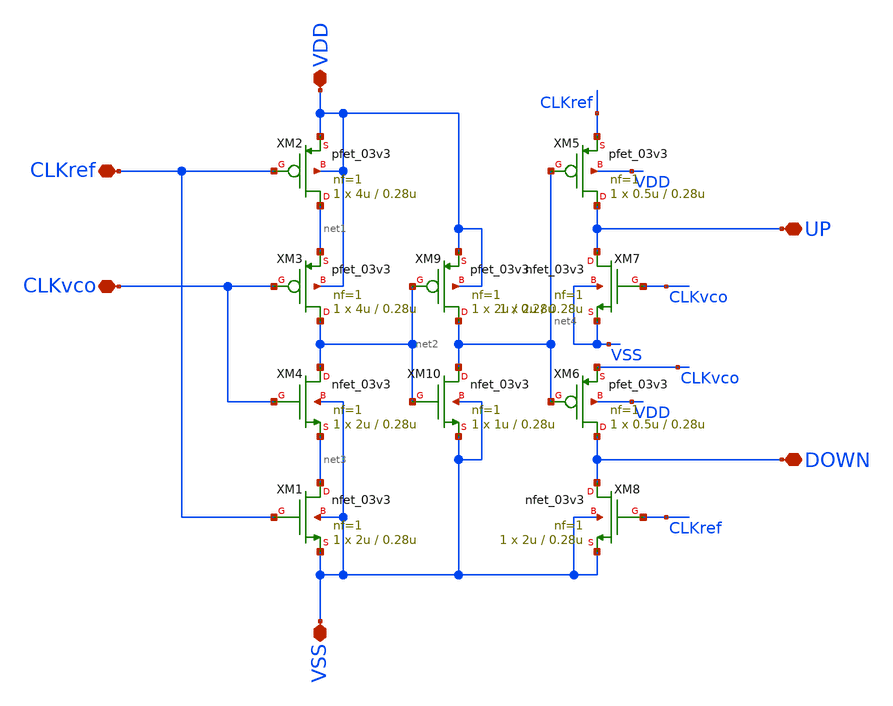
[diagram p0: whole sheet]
** sch_path: designs/libs/qw_core_analog/PFD_0deadzone.sch
**.subckt PFD_0deadzone CLKref CLKvco VSS VDD UP DOWN
*.iopin CLKref
*.iopin CLKvco
*.iopin VSS
*.iopin VDD
*.iopin UP
*.iopin DOWN
XM1 net3 CLKref VSS VSS nfet_03v3 L=0.28u W=2u nf=1 ad='int((nf+1)/2) * W/nf * 0.18u' as='int((nf+2)/2) * W/nf * 0.18u'
+ pd='2*int((nf+1)/2) * (W/nf + 0.18u)' ps='2*int((nf+2)/2) * (W/nf + 0.18u)' nrd='0.18u / W' nrs='0.18u / W'
+ sa=0 sb=0 sd=0 m=1
XM2 net1 CLKref VDD VDD pfet_03v3 L=0.28u W=4u nf=1 ad='int((nf+1)/2) * W/nf * 0.18u' as='int((nf+2)/2) * W/nf * 0.18u'
+ pd='2*int((nf+1)/2) * (W/nf + 0.18u)' ps='2*int((nf+2)/2) * (W/nf + 0.18u)' nrd='0.18u / W' nrs='0.18u / W'
+ sa=0 sb=0 sd=0 m=1
XM3 net2 CLKvco net1 VDD pfet_03v3 L=0.28u W=4u nf=1 ad='int((nf+1)/2) * W/nf * 0.18u' as='int((nf+2)/2) * W/nf * 0.18u'
+ pd='2*int((nf+1)/2) * (W/nf + 0.18u)' ps='2*int((nf+2)/2) * (W/nf + 0.18u)' nrd='0.18u / W' nrs='0.18u / W'
+ sa=0 sb=0 sd=0 m=1
XM4 net2 CLKvco net3 VSS nfet_03v3 L=0.28u W=2u nf=1 ad='int((nf+1)/2) * W/nf * 0.18u' as='int((nf+2)/2) * W/nf * 0.18u'
+ pd='2*int((nf+1)/2) * (W/nf + 0.18u)' ps='2*int((nf+2)/2) * (W/nf + 0.18u)' nrd='0.18u / W' nrs='0.18u / W'
+ sa=0 sb=0 sd=0 m=1
XM7 UP CLKvco VSS VSS nfet_03v3 L=0.28u W=2u nf=1 ad='int((nf+1)/2) * W/nf * 0.18u' as='int((nf+2)/2) * W/nf * 0.18u'
+ pd='2*int((nf+1)/2) * (W/nf + 0.18u)' ps='2*int((nf+2)/2) * (W/nf + 0.18u)' nrd='0.18u / W' nrs='0.18u / W'
+ sa=0 sb=0 sd=0 m=1
XM8 DOWN CLKref VSS VSS nfet_03v3 L=0.28u W=2u nf=1 ad='int((nf+1)/2) * W/nf * 0.18u' as='int((nf+2)/2) * W/nf * 0.18u'
+ pd='2*int((nf+1)/2) * (W/nf + 0.18u)' ps='2*int((nf+2)/2) * (W/nf + 0.18u)' nrd='0.18u / W' nrs='0.18u / W'
+ sa=0 sb=0 sd=0 m=1
XM5 UP net4 CLKref VDD pfet_03v3 L=0.28u W=0.5u nf=1 ad='int((nf+1)/2) * W/nf * 0.18u' as='int((nf+2)/2) * W/nf * 0.18u'
+ pd='2*int((nf+1)/2) * (W/nf + 0.18u)' ps='2*int((nf+2)/2) * (W/nf + 0.18u)' nrd='0.18u / W' nrs='0.18u / W'
+ sa=0 sb=0 sd=0 m=1
XM6 DOWN net4 CLKvco VDD pfet_03v3 L=0.28u W=0.5u nf=1 ad='int((nf+1)/2) * W/nf * 0.18u' as='int((nf+2)/2) * W/nf * 0.18u'
+ pd='2*int((nf+1)/2) * (W/nf + 0.18u)' ps='2*int((nf+2)/2) * (W/nf + 0.18u)' nrd='0.18u / W' nrs='0.18u / W'
+ sa=0 sb=0 sd=0 m=1
XM9 net4 net2 VDD VDD pfet_03v3 L=0.28u W=2u nf=1 ad='int((nf+1)/2) * W/nf * 0.18u' as='int((nf+2)/2) * W/nf * 0.18u'
+ pd='2*int((nf+1)/2) * (W/nf + 0.18u)' ps='2*int((nf+2)/2) * (W/nf + 0.18u)' nrd='0.18u / W' nrs='0.18u / W'
+ sa=0 sb=0 sd=0 m=1
XM10 net4 net2 VSS VSS nfet_03v3 L=0.28u W=1u nf=1 ad='int((nf+1)/2) * W/nf * 0.18u' as='int((nf+2)/2) * W/nf * 0.18u'
+ pd='2*int((nf+1)/2) * (W/nf + 0.18u)' ps='2*int((nf+2)/2) * (W/nf + 0.18u)' nrd='0.18u / W' nrs='0.18u / W'
+ sa=0 sb=0 sd=0 m=1
**.ends
.end
